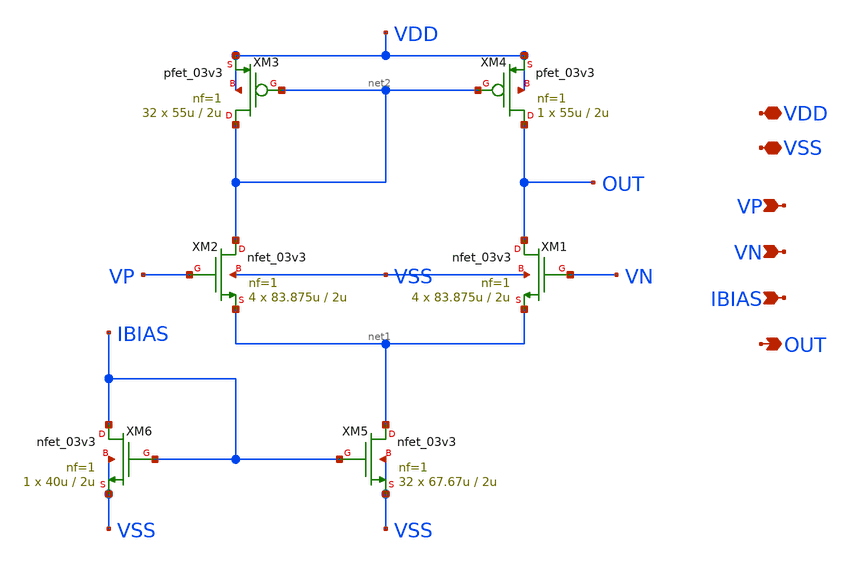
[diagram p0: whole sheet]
** sch_path: w1_advanced-foundation/w1_task/w1_tb/5t-ota.sch
**.subckt 5t-ota VDD VSS VP VN IBIAS OUT
*.iopin VDD
*.iopin VSS
*.ipin VP
*.ipin VN
*.ipin IBIAS
*.opin OUT
XM1 OUT VN net1 VSS nfet_03v3 L=2u W=83.875u nf=1 ad='int((nf+1)/2) * W/nf * 0.18u' as='int((nf+2)/2) * W/nf * 0.18u'
+ pd='2*int((nf+1)/2) * (W/nf + 0.18u)' ps='2*int((nf+2)/2) * (W/nf + 0.18u)' nrd='0.18u / W' nrs='0.18u / W'
+ sa=0 sb=0 sd=0 m=4
XM2 net2 VP net1 VSS nfet_03v3 L=2u W=83.875u nf=1 ad='int((nf+1)/2) * W/nf * 0.18u' as='int((nf+2)/2) * W/nf * 0.18u'
+ pd='2*int((nf+1)/2) * (W/nf + 0.18u)' ps='2*int((nf+2)/2) * (W/nf + 0.18u)' nrd='0.18u / W' nrs='0.18u / W'
+ sa=0 sb=0 sd=0 m=4
XM3 net2 net2 VDD VDD pfet_03v3 L=2u W=55u nf=1 ad='int((nf+1)/2) * W/nf * 0.18u' as='int((nf+2)/2) * W/nf * 0.18u'
+ pd='2*int((nf+1)/2) * (W/nf + 0.18u)' ps='2*int((nf+2)/2) * (W/nf + 0.18u)' nrd='0.18u / W' nrs='0.18u / W'
+ sa=0 sb=0 sd=0 m=32
XM4 OUT net2 VDD VDD pfet_03v3 L=2u W=55u nf=1 ad='int((nf+1)/2) * W/nf * 0.18u' as='int((nf+2)/2) * W/nf * 0.18u'
+ pd='2*int((nf+1)/2) * (W/nf + 0.18u)' ps='2*int((nf+2)/2) * (W/nf + 0.18u)' nrd='0.18u / W' nrs='0.18u / W'
+ sa=0 sb=0 sd=0 m=1
XM5 net1 IBIAS VSS VSS nfet_03v3 L=2u W=67.67u nf=1 ad='int((nf+1)/2) * W/nf * 0.18u' as='int((nf+2)/2) * W/nf * 0.18u'
+ pd='2*int((nf+1)/2) * (W/nf + 0.18u)' ps='2*int((nf+2)/2) * (W/nf + 0.18u)' nrd='0.18u / W' nrs='0.18u / W'
+ sa=0 sb=0 sd=0 m=32
XM6 IBIAS IBIAS VSS VSS nfet_03v3 L=2u W=40u nf=1 ad='int((nf+1)/2) * W/nf * 0.18u' as='int((nf+2)/2) * W/nf * 0.18u'
+ pd='2*int((nf+1)/2) * (W/nf + 0.18u)' ps='2*int((nf+2)/2) * (W/nf + 0.18u)' nrd='0.18u / W' nrs='0.18u / W'
+ sa=0 sb=0 sd=0 m=1
**.ends
.end
